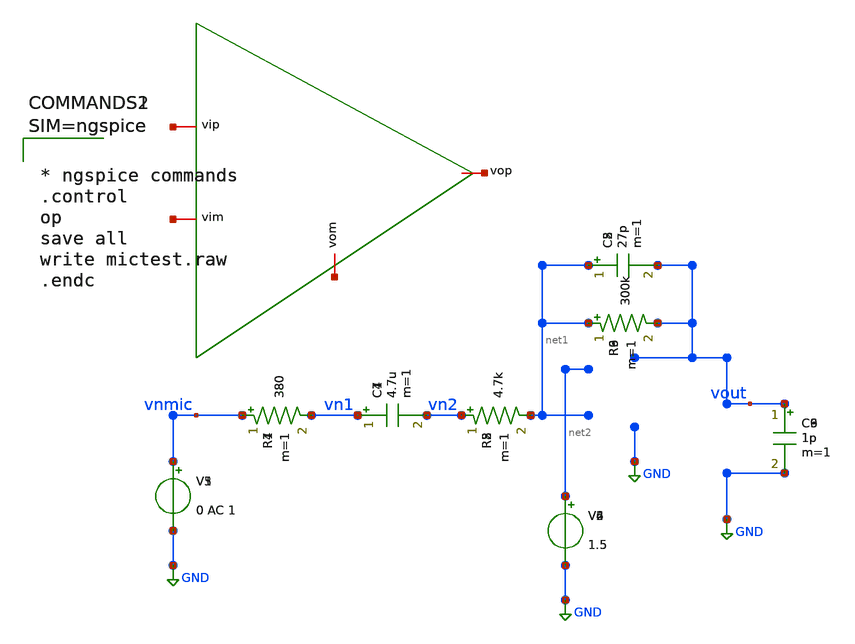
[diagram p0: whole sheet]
** sch_path: xschem/op.sch
**.subckt op
V1 vnmic GND 0 AC 1
R1 vnmic vn1 380 m=1
C1 vn1 vn2 4.7u m=1
R2 vn2 net1 4.7k m=1
R3 net1 vout 300k m=1
C2 net1 vout 27p m=1
C3 vout GND 1p m=1
V2 net2 GND 1.5
V3 vnmic GND 0 AC 1
R4 vnmic vn1 380 m=1
C4 vn1 vn2 4.7u m=1
R5 vn2 net1 4.7k m=1
R6 net1 vout 300k m=1
C5 net1 vout 27p m=1
C6 vout GND 1p m=1
V4 net2 GND 1.5
V5 vnmic GND 0 AC 1
R7 vnmic vn1 380 m=1
C7 vn1 vn2 4.7u m=1
R8 vn2 net1 4.7k m=1
R9 net1 vout 300k m=1
C8 net1 vout 27p m=1
C9 vout GND 1p m=1
V6 net2 GND 1.5
**** begin user architecture code



* ngspice commands
.control
op
save all
write mictest.raw
.endc






* ngspice commands
.control
op
save all
write mictest.raw
.endc






* ngspice commands
.control
op
save all
write mictest.raw
.endc



**** end user architecture code
**.ends
.GLOBAL GND
.end
